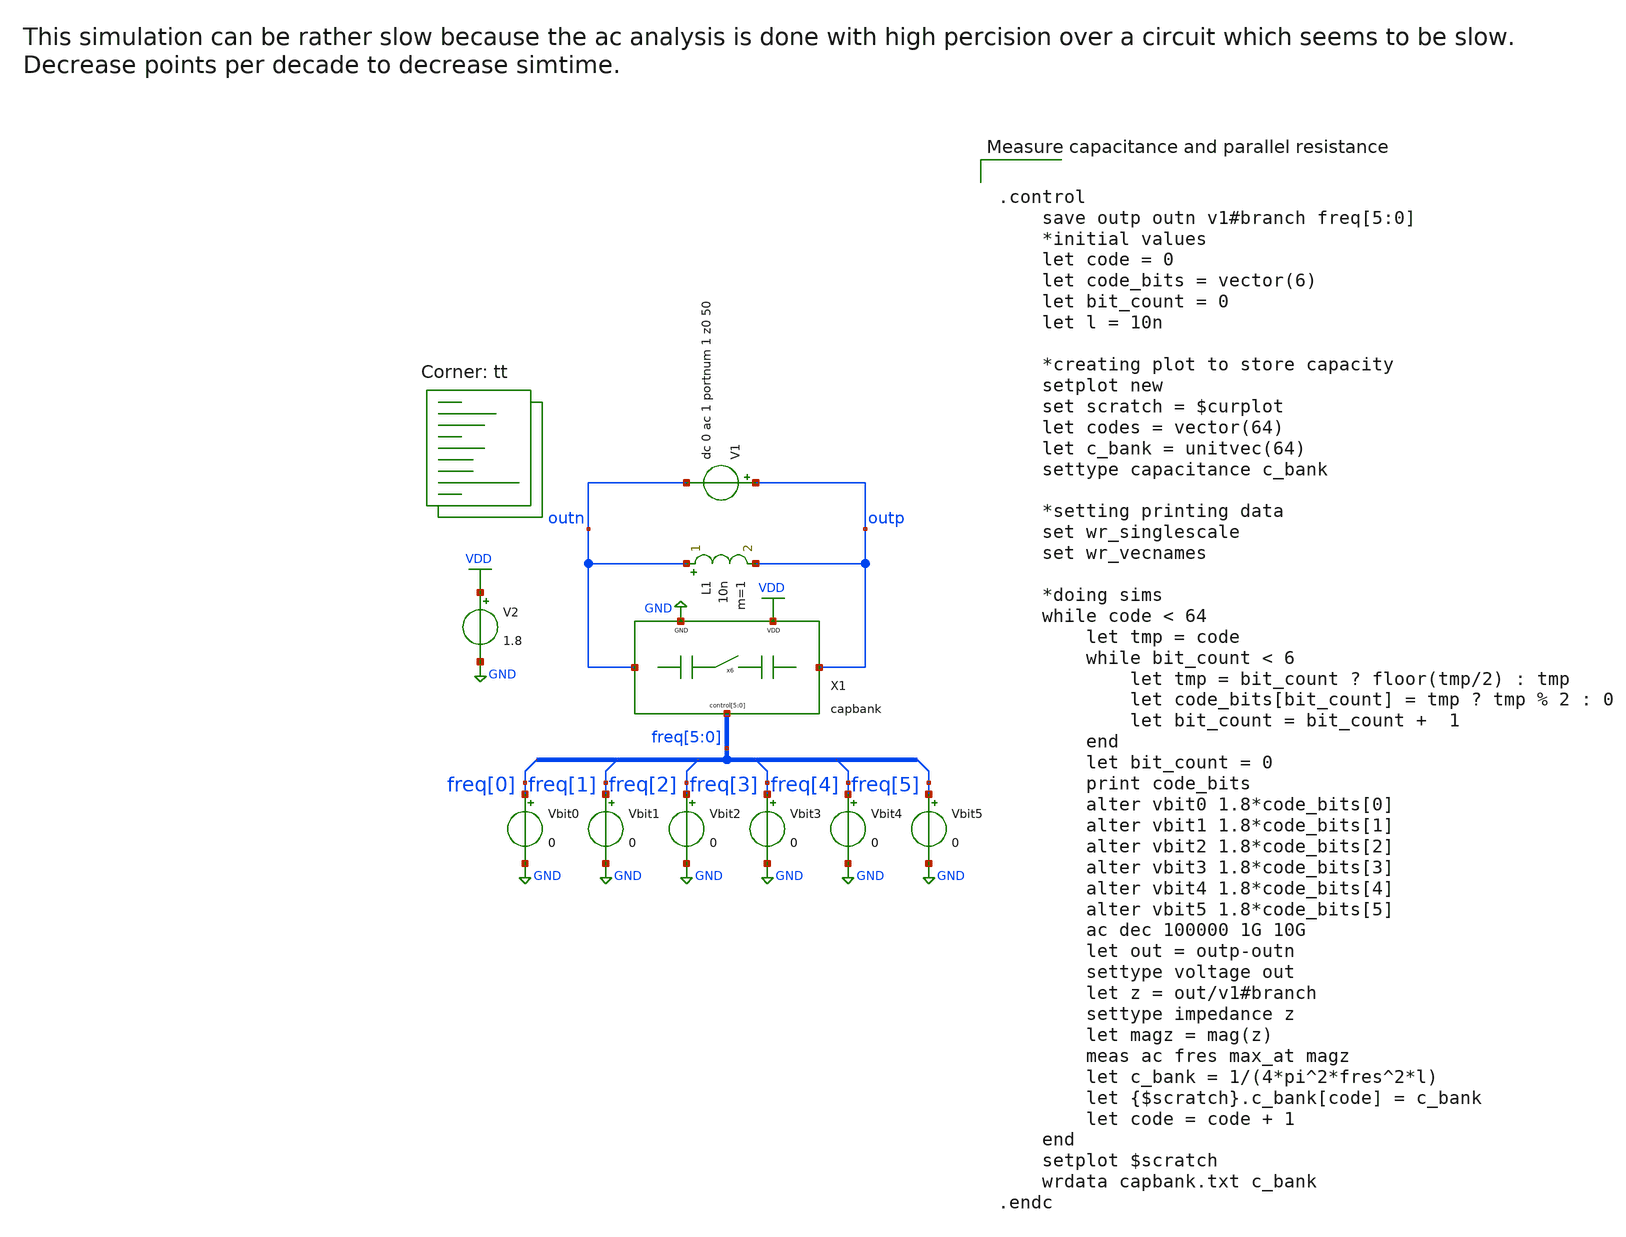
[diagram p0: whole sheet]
** sch_path: xschem/vco/testbenches/capbank/capbank_capacity_measurement_tb.sch
**.subckt capbank_capacity_measurement_tb
X1 outn outp VDD freq[5] freq[4] freq[3] freq[2] freq[1] freq[0] GND capbank
L1 outn outp 10n m=1
Vbit0 freq[0] GND 0
Vbit1 freq[1] GND 0
Vbit2 freq[2] GND 0
Vbit3 freq[3] GND 0
Vbit4 freq[4] GND 0
Vbit5 freq[5] GND 0
V1 outp outn dc 0 ac 1 portnum 1 z0 50
V2 VDD GND 1.8
**** begin user architecture code
.lib $::SKYWATER_MODELS/sky130.lib.spice tt


.control
    save outp outn v1#branch freq[5:0]
    *initial values
    let code = 0
    let code_bits = vector(6)
    let bit_count = 0
    let l = 10n

    *creating plot to store capacity
    setplot new
    set scratch = $curplot
    let codes = vector(64)
    let c_bank = unitvec(64)
    settype capacitance c_bank

    *setting printing data
    set wr_singlescale
    set wr_vecnames

    *doing sims
    while code < 64
        let tmp = code
        while bit_count < 6
            let tmp = bit_count ? floor(tmp/2) : tmp
            let code_bits[bit_count] = tmp ? tmp % 2 : 0
            let bit_count = bit_count +  1
        end
        let bit_count = 0
        print code_bits
        alter vbit0 1.8*code_bits[0]
        alter vbit1 1.8*code_bits[1]
        alter vbit2 1.8*code_bits[2]
        alter vbit3 1.8*code_bits[3]
        alter vbit4 1.8*code_bits[4]
        alter vbit5 1.8*code_bits[5]
        ac dec 100000 1G 10G
        let out = outp-outn
        settype voltage out
        let z = out/v1#branch
        settype impedance z
        let magz = mag(z)
        meas ac fres max_at magz
        let c_bank = 1/(4*pi^2*fres^2*l)
        let {$scratch}.c_bank[code] = c_bank
        let code = code + 1
    end
    setplot $scratch
    wrdata capbank.txt c_bank
.endc


**** end user architecture code
**.ends
.GLOBAL VDD
.GLOBAL GND
.end
